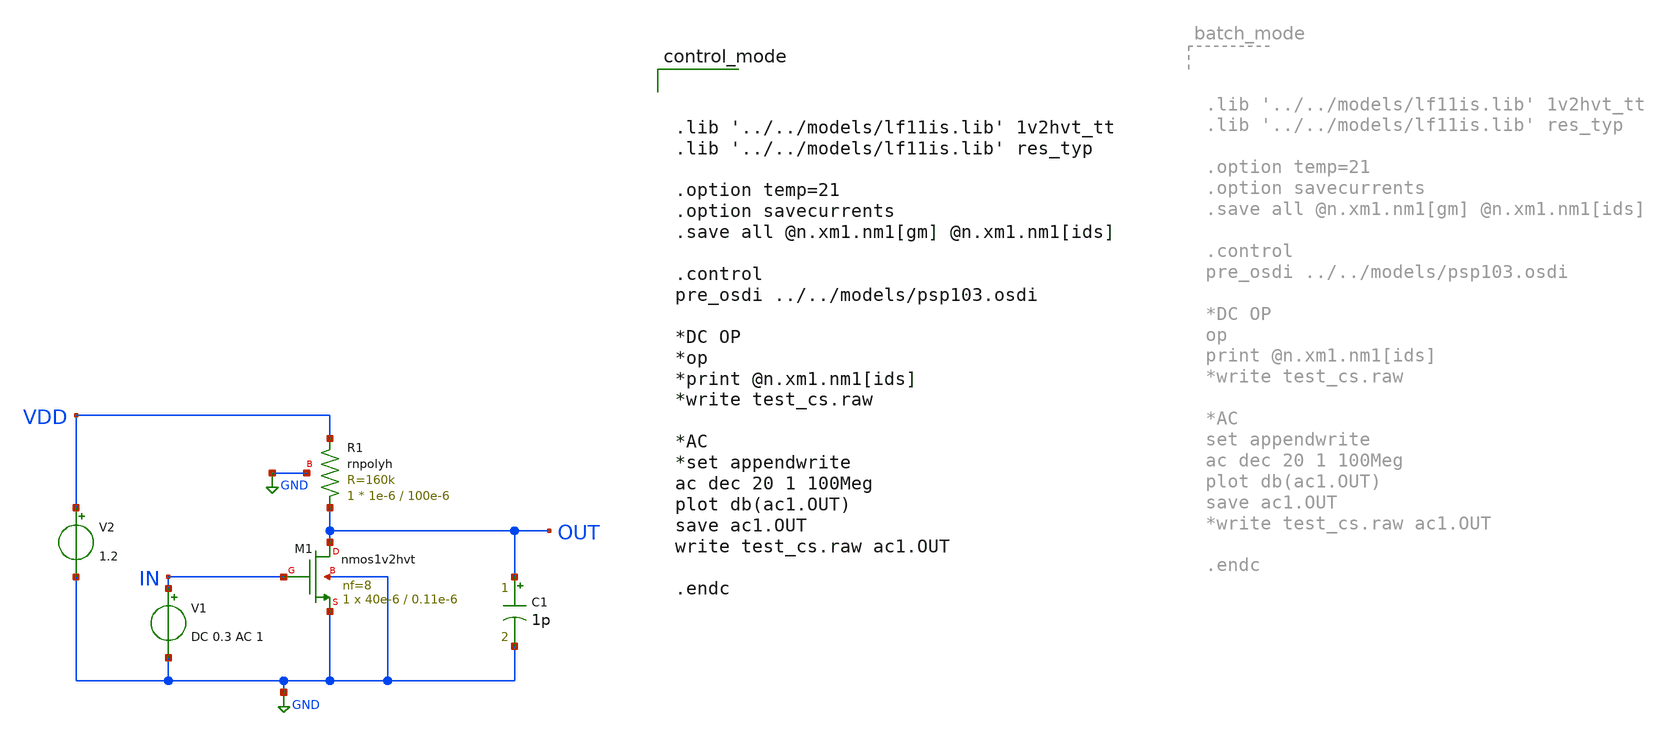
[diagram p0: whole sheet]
** sch_path: test_cs.sch
**.subckt test_cs
XM1 OUT IN GND GND nmos1v2hvt L=0.11e-6 W=40e-6 nf=8 abdrain='int((nf+1)/2) * W/nf * 0.29' absource='int((nf+2)/2) * W/nf * 0.29'
+ lsdrain='2*int((nf+1)/2) * (W/nf + 0.29)' lssource='2*int((nf+2)/2) * (W/nf + 0.29)' dta=0 nrd='0.29 / W'
+ nrs='0.29 / W' sa=0 sb=0 sd=0 mult=1 m=1
XR1 OUT VDD GND rnpolyh w=1e-6 l=100e-6 m=1
V1 IN GND DC 0.3 AC 1
V2 VDD GND 1.2
C1 OUT GND 1p m=1
**** begin user architecture code



.lib '../../models/lf11is.lib' 1v2hvt_tt
.lib '../../models/lf11is.lib' res_typ

.option temp=21
.option savecurrents
.save all @n.xm1.nm1[gm] @n.xm1.nm1[ids]

.control
pre_osdi ../../models/psp103.osdi

*DC OP
*op
*print @n.xm1.nm1[ids]
*write test_cs.raw

*AC
*set appendwrite
ac dec 20 1 100Meg
plot db(ac1.OUT)
save ac1.OUT
write test_cs.raw ac1.OUT

.endc



**** end user architecture code
**.ends
.GLOBAL GND
.end
